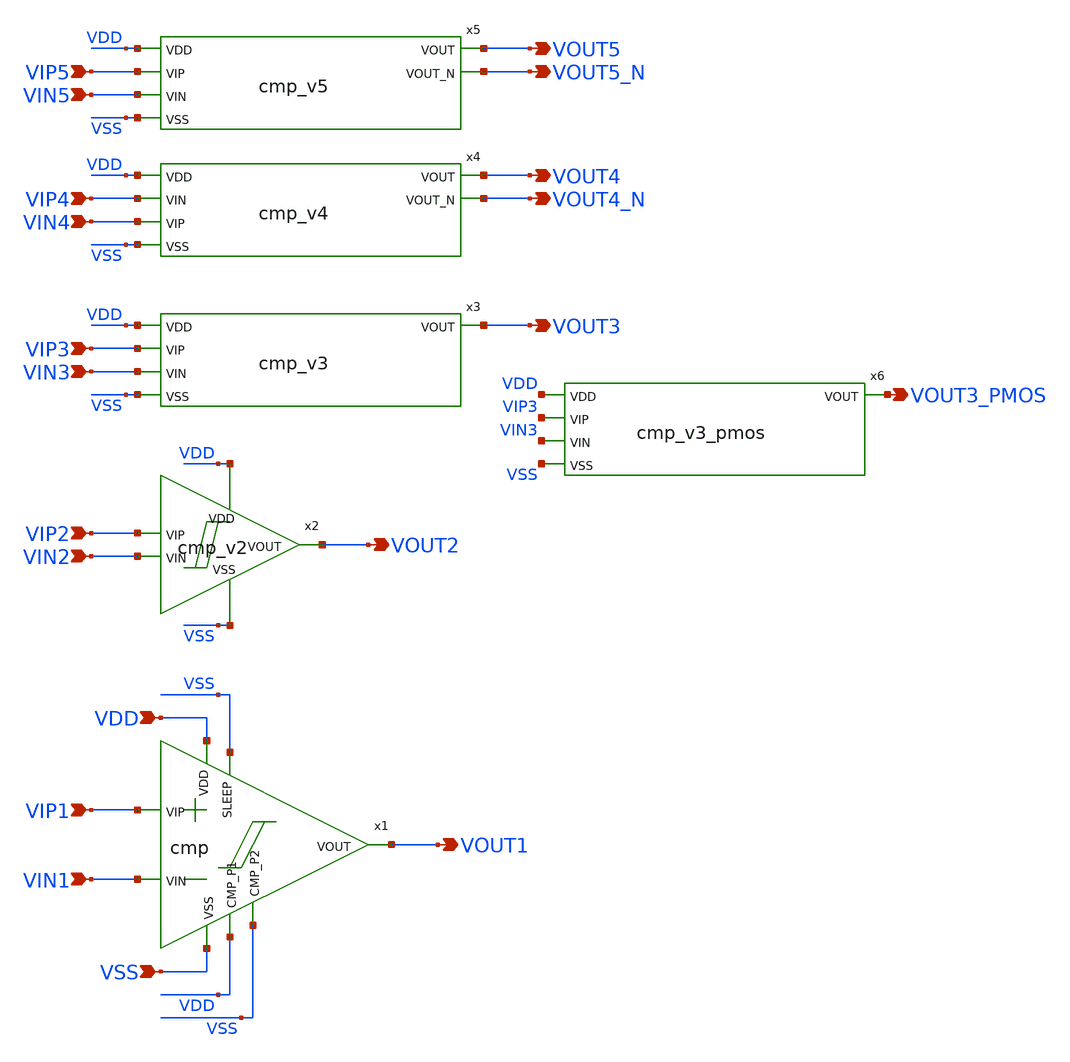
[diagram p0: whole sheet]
** sch_path: design/LELO_TORD_SKY130A/TB_cmps.sch
**.subckt TB_cmps VOUT1 VOUT2 VOUT3 VDD VSS VIP1 VIN1 VIP2 VIN2 VIP3 VIN3 VOUT4 VOUT4_N VIP4 VIN4
*+ VIP5 VIN5 VOUT5 VOUT5_N VOUT3_PMOS
*.opin VOUT1
*.opin VOUT2
*.opin VOUT3
*.ipin VDD
*.ipin VSS
*.ipin VIP1
*.ipin VIN1
*.ipin VIP2
*.ipin VIN2
*.ipin VIP3
*.ipin VIN3
*.opin VOUT4
*.opin VOUT4_N
*.ipin VIP4
*.ipin VIN4
*.ipin VIP5
*.ipin VIN5
*.opin VOUT5
*.opin VOUT5_N
*.opin VOUT3_PMOS
x1 VDD VSS VSS VDD VIP1 VIN1 VOUT1 VSS cmp
x2 VDD VIP2 VIN2 VOUT2 VSS cmp_v2
x3 VDD VIP3 VIN3 VOUT3 VSS cmp_v3
x4 VDD VOUT4 VIP4 VIN4 VOUT4_N VSS cmp_v4
x5 VDD VOUT5 VIP5 VIN5 VOUT5_N VSS cmp_v5
x6 VDD VIP3 VIN3 VOUT3_PMOS VSS cmp_v3_pmos
**.ends
.end
